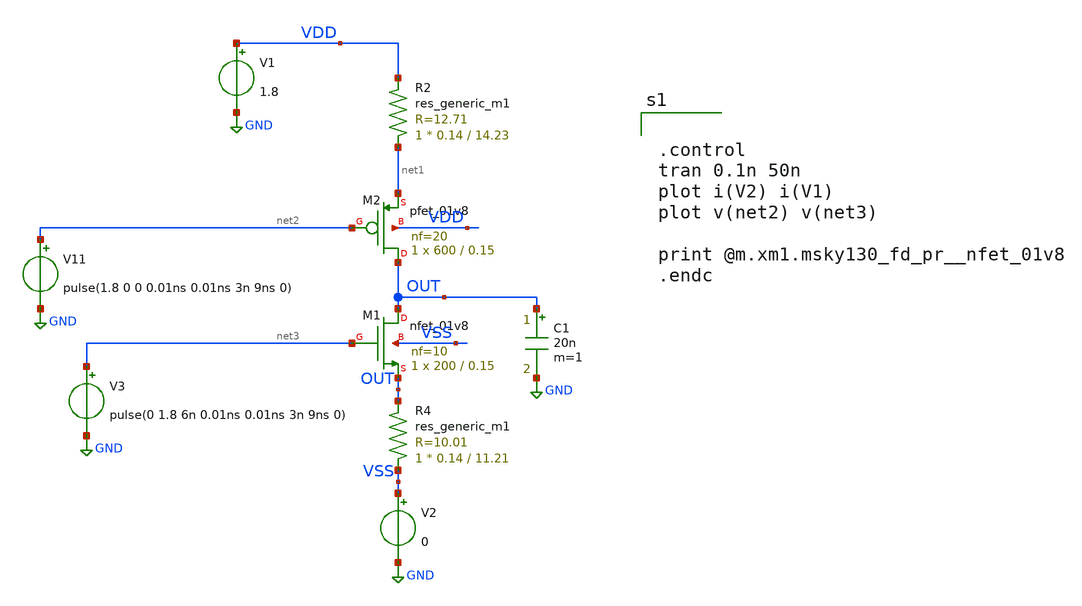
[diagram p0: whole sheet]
** sch_path: xschem/DC_DC_Converter_xschem/DC_DC_Converter/current_pump/current_pump_copy.sch
**.subckt current_pump_copy
XM1 OUT net3 OUT VSS sky130_fd_pr__nfet_01v8 L=0.15 W=200 nf=10 ad='int((nf+1)/2) * W/nf * 0.29' as='int((nf+2)/2) * W/nf * 0.29'
+ pd='2*int((nf+1)/2) * (W/nf + 0.29)' ps='2*int((nf+2)/2) * (W/nf + 0.29)' nrd='0.29 / W' nrs='0.29 / W'
+ sa=0 sb=0 sd=0 mult=1 m=1
XM2 OUT net2 net1 VDD sky130_fd_pr__pfet_01v8 L=0.15 W=600 nf=20 ad='int((nf+1)/2) * W/nf * 0.29' as='int((nf+2)/2) * W/nf * 0.29'
+ pd='2*int((nf+1)/2) * (W/nf + 0.29)' ps='2*int((nf+2)/2) * (W/nf + 0.29)' nrd='0.29 / W' nrs='0.29 / W'
+ sa=0 sb=0 sd=0 mult=1 m=1
C1 OUT GND 20n m=1
V1 VDD GND 1.8
V2 VSS GND 0
V11 net2 GND pulse(1.8 0 0 0.01ns 0.01ns 3n 9ns 0)
V3 net3 GND pulse(0 1.8 6n 0.01ns 0.01ns 3n 9ns 0)
R2 net1 VDD sky130_fd_pr__res_generic_m1 W=0.14 L=14.23 m=1
R4 VSS OUT sky130_fd_pr__res_generic_m1 W=0.14 L=11.21 m=1
**** begin user architecture code


.control
tran 0.1n 50n
plot i(V2) i(V1)
plot v(net2) v(net3)

print @m.xm1.msky130_fd_pr__nfet_01v8
.endc



** opencircuitdesign pdks install
.lib $::SKYWATER_MODELS/sky130.lib.spice tt


**** end user architecture code
**.ends
.GLOBAL GND
.end
